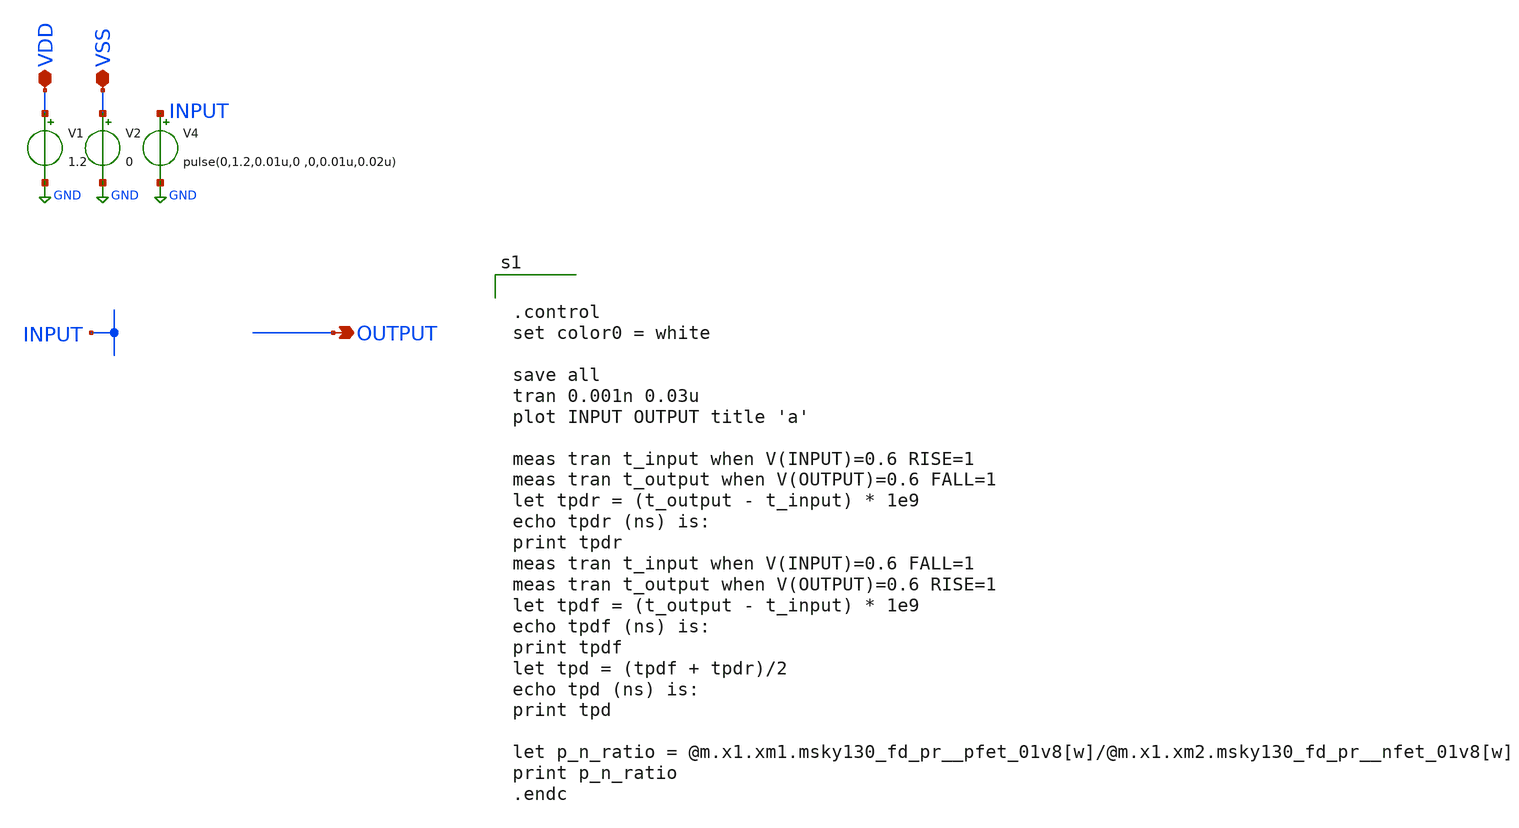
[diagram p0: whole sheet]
** sch_path: design/xschem/NAND/nand_TB.sch
**.subckt nand_TB OUTPUT VDD VSS
*.opin OUTPUT
*.iopin VDD
*.iopin VSS
V1 VDD GND 1.2
V2 VSS GND 0
V4 INPUT GND pulse(0,1.2,0.01u,0 ,0,0.01u,0.02u)
**** begin user architecture code

** opencircuitdesign pdks install
.lib $::SKYWATER_MODELS/sky130.lib.spice tt_mm




.control
set color0 = white

save all
tran 0.001n 0.03u
plot INPUT OUTPUT title 'a'

meas tran t_input when V(INPUT)=0.6 RISE=1
meas tran t_output when V(OUTPUT)=0.6 FALL=1
let tpdr = (t_output - t_input) * 1e9
echo tpdr (ns) is:
print tpdr
meas tran t_input when V(INPUT)=0.6 FALL=1
meas tran t_output when V(OUTPUT)=0.6 RISE=1
let tpdf = (t_output - t_input) * 1e9
echo tpdf (ns) is:
print tpdf
let tpd = (tpdf + tpdr)/2
echo tpd (ns) is:
print tpd

let p_n_ratio = @m.x1.xm1.msky130_fd_pr__pfet_01v8[w]/@m.x1.xm2.msky130_fd_pr__nfet_01v8[w]
print p_n_ratio
.endc


**** end user architecture code
**.ends
.GLOBAL GND
.end
